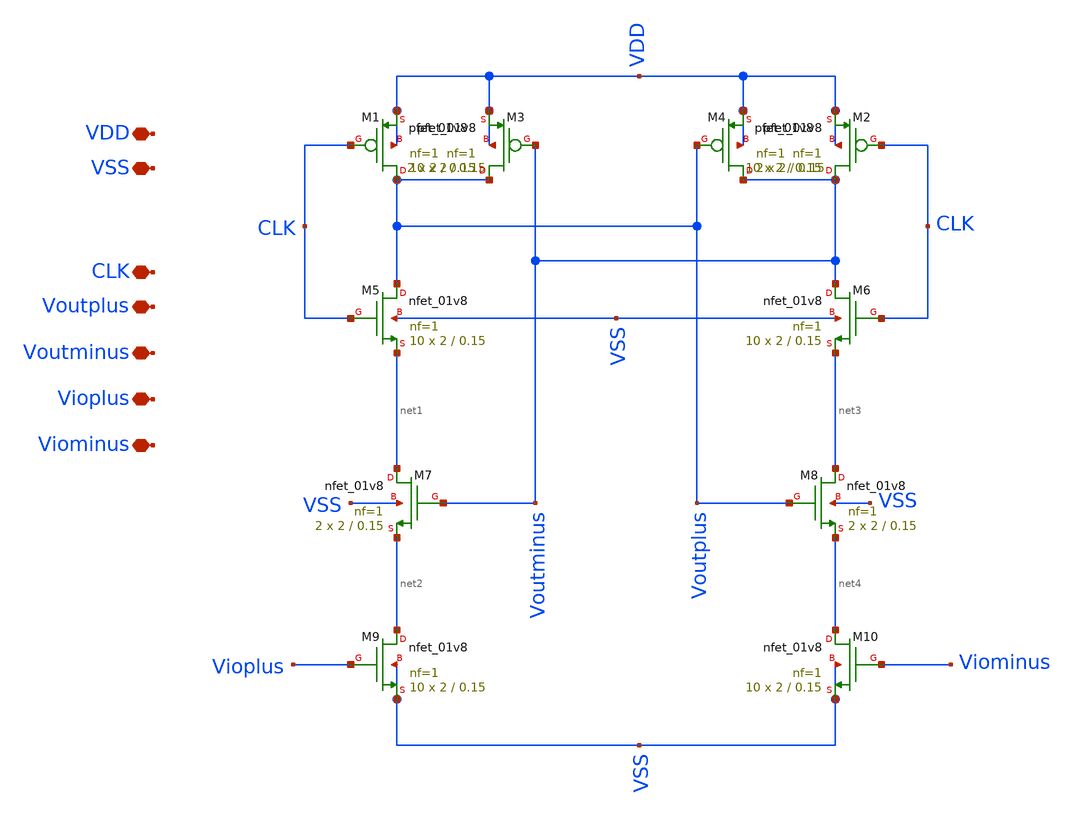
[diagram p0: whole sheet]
** sch_path: xschem/combination_test_WORKING.sch
**.subckt combination_test_WORKING VDD VSS CLK Voutplus Voutminus Vioplus Viominus
*.iopin VDD
*.iopin VSS
*.iopin CLK
*.iopin Voutplus
*.iopin Voutminus
*.iopin Vioplus
*.iopin Viominus
XM1 Voutplus CLK VDD VDD sky130_fd_pr__pfet_01v8 L=0.15 W=2 nf=1 ad='int((nf+1)/2) * W/nf * 0.29' as='int((nf+2)/2) * W/nf * 0.29'
+ pd='2*int((nf+1)/2) * (W/nf + 0.29)' ps='2*int((nf+2)/2) * (W/nf + 0.29)' nrd='0.29 / W' nrs='0.29 / W'
+ sa=0 sb=0 sd=0 mult=10 m=10
XM2 Voutminus CLK VDD VDD sky130_fd_pr__pfet_01v8 L=0.15 W=2 nf=1 ad='int((nf+1)/2) * W/nf * 0.29' as='int((nf+2)/2) * W/nf * 0.29'
+ pd='2*int((nf+1)/2) * (W/nf + 0.29)' ps='2*int((nf+2)/2) * (W/nf + 0.29)' nrd='0.29 / W' nrs='0.29 / W'
+ sa=0 sb=0 sd=0 mult=10 m=10
XM3 Voutplus Voutminus VDD VDD sky130_fd_pr__pfet_01v8 L=0.15 W=2 nf=1 ad='int((nf+1)/2) * W/nf * 0.29'
+ as='int((nf+2)/2) * W/nf * 0.29' pd='2*int((nf+1)/2) * (W/nf + 0.29)' ps='2*int((nf+2)/2) * (W/nf + 0.29)'
+ nrd='0.29 / W' nrs='0.29 / W' sa=0 sb=0 sd=0 mult=2 m=2
XM4 Voutminus Voutplus VDD VDD sky130_fd_pr__pfet_01v8 L=0.15 W=2 nf=1 ad='int((nf+1)/2) * W/nf * 0.29'
+ as='int((nf+2)/2) * W/nf * 0.29' pd='2*int((nf+1)/2) * (W/nf + 0.29)' ps='2*int((nf+2)/2) * (W/nf + 0.29)'
+ nrd='0.29 / W' nrs='0.29 / W' sa=0 sb=0 sd=0 mult=2 m=2
XM5 Voutplus CLK net1 VSS sky130_fd_pr__nfet_01v8 L=0.15 W=2 nf=1 ad='int((nf+1)/2) * W/nf * 0.29' as='int((nf+2)/2) * W/nf * 0.29'
+ pd='2*int((nf+1)/2) * (W/nf + 0.29)' ps='2*int((nf+2)/2) * (W/nf + 0.29)' nrd='0.29 / W' nrs='0.29 / W'
+ sa=0 sb=0 sd=0 mult=10 m=10
XM6 Voutminus CLK net3 VSS sky130_fd_pr__nfet_01v8 L=0.15 W=2 nf=1 ad='int((nf+1)/2) * W/nf * 0.29' as='int((nf+2)/2) * W/nf * 0.29'
+ pd='2*int((nf+1)/2) * (W/nf + 0.29)' ps='2*int((nf+2)/2) * (W/nf + 0.29)' nrd='0.29 / W' nrs='0.29 / W'
+ sa=0 sb=0 sd=0 mult=10 m=10
XM7 net1 Voutminus net2 VSS sky130_fd_pr__nfet_01v8 L=0.15 W=2 nf=1 ad='int((nf+1)/2) * W/nf * 0.29'
+ as='int((nf+2)/2) * W/nf * 0.29' pd='2*int((nf+1)/2) * (W/nf + 0.29)' ps='2*int((nf+2)/2) * (W/nf + 0.29)'
+ nrd='0.29 / W' nrs='0.29 / W' sa=0 sb=0 sd=0 mult=2 m=2
XM8 net3 Voutplus net4 VSS sky130_fd_pr__nfet_01v8 L=0.15 W=2 nf=1 ad='int((nf+1)/2) * W/nf * 0.29' as='int((nf+2)/2) * W/nf * 0.29'
+ pd='2*int((nf+1)/2) * (W/nf + 0.29)' ps='2*int((nf+2)/2) * (W/nf + 0.29)' nrd='0.29 / W' nrs='0.29 / W'
+ sa=0 sb=0 sd=0 mult=2 m=2
XM9 net2 Vioplus VSS VSS sky130_fd_pr__nfet_01v8 L=0.15 W=2 nf=1 ad='int((nf+1)/2) * W/nf * 0.29' as='int((nf+2)/2) * W/nf * 0.29'
+ pd='2*int((nf+1)/2) * (W/nf + 0.29)' ps='2*int((nf+2)/2) * (W/nf + 0.29)' nrd='0.29 / W' nrs='0.29 / W'
+ sa=0 sb=0 sd=0 mult=10 m=10
XM10 net4 Viominus VSS VSS sky130_fd_pr__nfet_01v8 L=0.15 W=2 nf=1 ad='int((nf+1)/2) * W/nf * 0.29' as='int((nf+2)/2) * W/nf * 0.29'
+ pd='2*int((nf+1)/2) * (W/nf + 0.29)' ps='2*int((nf+2)/2) * (W/nf + 0.29)' nrd='0.29 / W' nrs='0.29 / W'
+ sa=0 sb=0 sd=0 mult=10 m=10
**.ends
.end
